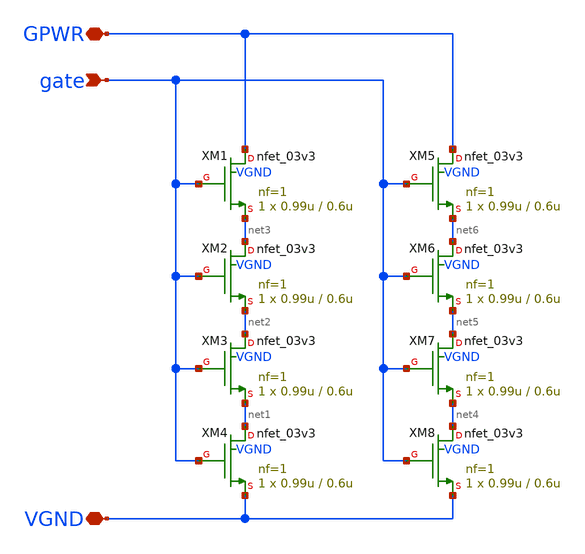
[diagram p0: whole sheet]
** sch_path: pg/gf180mcuD/common/xschem/discharge_3v3.sch
**.subckt discharge_3v3 GPWR VGND gate
*.iopin GPWR
*.iopin VGND
*.ipin gate
XM1 GPWR gate net3 VGND nfet_03v3 L=0.6u W=0.99u nf=1 ad='int((nf+1)/2) * W/nf * 0.18u' as='int((nf+2)/2) * W/nf * 0.18u'
+ pd='2*int((nf+1)/2) * (W/nf + 0.18u)' ps='2*int((nf+2)/2) * (W/nf + 0.18u)' nrd='0.18u / W' nrs='0.18u / W'
+ sa=0 sb=0 sd=0 m=1 par=1
XM2 net3 gate net2 VGND nfet_03v3 L=0.6u W=0.99u nf=1 ad='int((nf+1)/2) * W/nf * 0.18u' as='int((nf+2)/2) * W/nf * 0.18u'
+ pd='2*int((nf+1)/2) * (W/nf + 0.18u)' ps='2*int((nf+2)/2) * (W/nf + 0.18u)' nrd='0.18u / W' nrs='0.18u / W'
+ sa=0 sb=0 sd=0 m=1 par=1
XM3 net2 gate net1 VGND nfet_03v3 L=0.6u W=0.99u nf=1 ad='int((nf+1)/2) * W/nf * 0.18u' as='int((nf+2)/2) * W/nf * 0.18u'
+ pd='2*int((nf+1)/2) * (W/nf + 0.18u)' ps='2*int((nf+2)/2) * (W/nf + 0.18u)' nrd='0.18u / W' nrs='0.18u / W'
+ sa=0 sb=0 sd=0 m=1 par=1
XM4 net1 gate VGND VGND nfet_03v3 L=0.6u W=0.99u nf=1 ad='int((nf+1)/2) * W/nf * 0.18u' as='int((nf+2)/2) * W/nf * 0.18u'
+ pd='2*int((nf+1)/2) * (W/nf + 0.18u)' ps='2*int((nf+2)/2) * (W/nf + 0.18u)' nrd='0.18u / W' nrs='0.18u / W'
+ sa=0 sb=0 sd=0 m=1 par=1
XM5 GPWR gate net6 VGND nfet_03v3 L=0.6u W=0.99u nf=1 ad='int((nf+1)/2) * W/nf * 0.18u' as='int((nf+2)/2) * W/nf * 0.18u'
+ pd='2*int((nf+1)/2) * (W/nf + 0.18u)' ps='2*int((nf+2)/2) * (W/nf + 0.18u)' nrd='0.18u / W' nrs='0.18u / W'
+ sa=0 sb=0 sd=0 m=1 par=1
XM6 net6 gate net5 VGND nfet_03v3 L=0.6u W=0.99u nf=1 ad='int((nf+1)/2) * W/nf * 0.18u' as='int((nf+2)/2) * W/nf * 0.18u'
+ pd='2*int((nf+1)/2) * (W/nf + 0.18u)' ps='2*int((nf+2)/2) * (W/nf + 0.18u)' nrd='0.18u / W' nrs='0.18u / W'
+ sa=0 sb=0 sd=0 m=1 par=1
XM7 net5 gate net4 VGND nfet_03v3 L=0.6u W=0.99u nf=1 ad='int((nf+1)/2) * W/nf * 0.18u' as='int((nf+2)/2) * W/nf * 0.18u'
+ pd='2*int((nf+1)/2) * (W/nf + 0.18u)' ps='2*int((nf+2)/2) * (W/nf + 0.18u)' nrd='0.18u / W' nrs='0.18u / W'
+ sa=0 sb=0 sd=0 m=1 par=1
XM8 net4 gate VGND VGND nfet_03v3 L=0.6u W=0.99u nf=1 ad='int((nf+1)/2) * W/nf * 0.18u' as='int((nf+2)/2) * W/nf * 0.18u'
+ pd='2*int((nf+1)/2) * (W/nf + 0.18u)' ps='2*int((nf+2)/2) * (W/nf + 0.18u)' nrd='0.18u / W' nrs='0.18u / W'
+ sa=0 sb=0 sd=0 m=1 par=1
**.ends
.end
